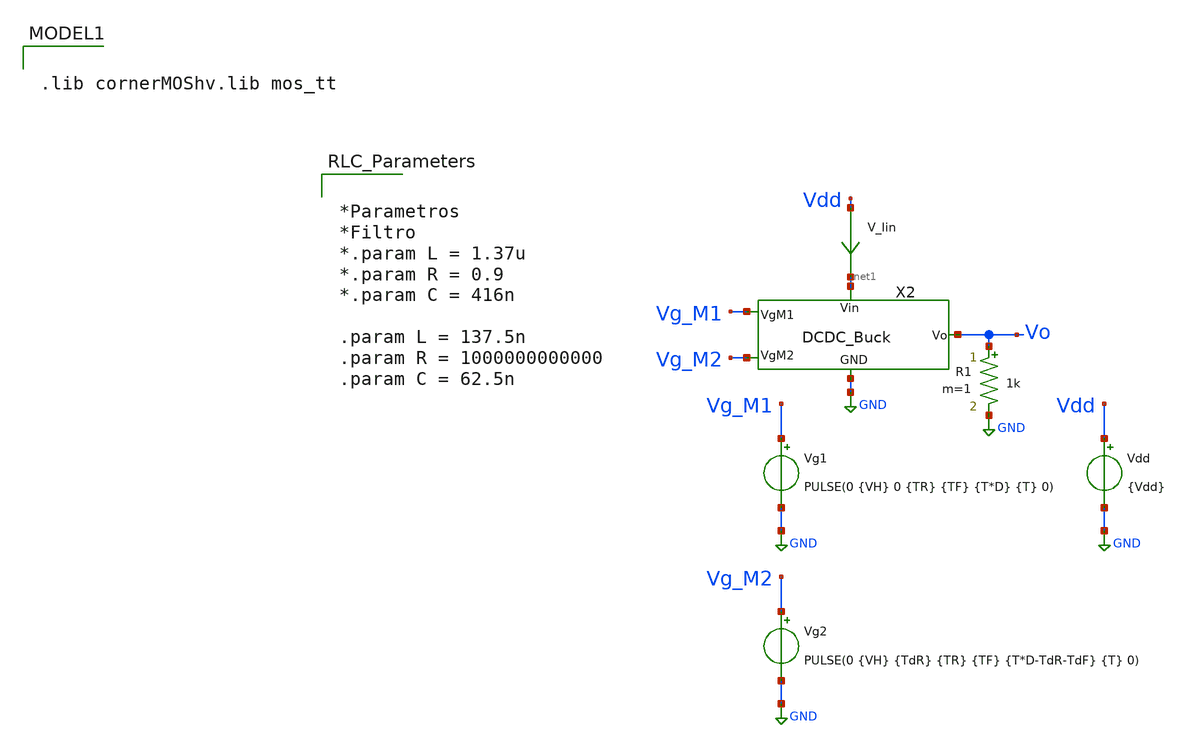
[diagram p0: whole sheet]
** sch_path: ChipUSM_AnalogTrack24/DCDCBuck/TB_DCDCBuck_SweepR.sch
**.subckt TB_DCDCBuck_SweepR
Vdd Vdd GND {Vdd}
Vg2 Vg_M2 GND PULSE(0 {VH} {TdR} {TR} {TF} {T*D-TdR-TdF} {T} 0)
Vg1 Vg_M1 GND PULSE(0 {VH} 0 {TR} {TF} {T*D} {T} 0)
V_Iin Vdd net1 0
.save i(v_iin)
R1 Vo GND 1k m=1
X2 Vg_M1 Vg_M2 net1 net2 Vo DCDC_Buck
**** begin user architecture code


.param temp=27
.param mult_M1 = 18000*2
.param w_M1 =10u
.param l_M1 = 0.4u
.param ng_M1 = 1

.param mult_M2 = 6000*2
.param w_M2 =10u
.param l_M2 =0.45u
.param ng_M2 =1







.param Vdd = 3.3
.param VH = 3.3
.param Del = 0

*.param D = 0.42
*.param T = 1u
*.param TR = 7n
*.param TF = 7n
*.param TdR = 0.1u
*.param TdF = 0.1u

*.param D = 0.6364
.param D = 0.55
.param T = 0.1u
.param TR = 10n
.param TF = 10n
.param TdR = 10n
.param TdF = 10n

.param temp = 27




.lib cornerMOShv.lib mos_tt



*Parametros
*Filtro
*.param L = 1.37u
*.param R = 0.9
*.param C = 416n

.param L = 137.5n
.param R = 1000000000000
.param C = 62.5n





.save all  @n.x1.xm1.nsg13_hv_pmos[ids]  @n.x1.xm2.nsg13_hv_nmos[ids]
.param SimTime = 5u
.param R = 0.6  ; Valor inicial de R

.control
reset
set color0 = white

* Barrido del parámetro R
foreach R_val 0.6 0.7 0.8 0.9 1.0 1.1 1.2
    print R_val
    alter R1 R_val  ; Cambiar el valor de R en cada iteración

    tran 1n 5u  ; Realizar la simulación transitoria

    let Io = i(v.x1.V_Io)
    let Id_M1 = @n.x1.xm1.nsg13_hv_pmos[ids]
    let Id_M2 = @n.x1.xm2.nsg13_hv_nmos[ids]
    let Po = Io*v(Vo)
    let I_in = i(V_Iin)
    let Pin = I_in*v(Vdd)
    let Vsd_M1 = v(Vdd) - v(x1.Vc)
    let Vds_M2 = v(x1.Vc)
    let P_M1 = Vsd_M1*Id_M1
    let P_M2 = -Vds_M2*Id_M2

    meas tran Vo_mean AVG v(Vo) from=4u to=5u
    meas tran Io_mean AVG Io from=4u to=5u
    meas tran Po_mean AVG Po from=4u to=5u
    meas tran Pin_mean AVG Pin from=4u to=5u
    meas tran P_M1_mean AVG P_M1 from=4u to=5u
    meas tran P_M2_mean AVG P_M2 from=4u to=5u

    let eff = 100*Po_mean/Pin_mean
    let loss_M1 = 100*P_M1_mean/Pin_mean
    let loss_M2 = 100*P_M2_mean/Pin_mean
    let sumaPot = eff + loss_M1 + loss_M2
    print eff loss_M1 loss_M2 sumaPot

    * Graficar los resultados por cada R_val
    plot Io i(v.x1.V_IL)
    *plot Id_M1 Id_M2
    *plot v(Vo)
    *plot Po Pin
    *plot v(x1.Vc)
    *plot v(Vg_M1) v(Vg_M2)

end  ; Fin del bucle foreach
.endc

.end





**** end user architecture code
**.ends

* expanding   symbol:
*+  /home/designer/shared/simulations/IHP-sg13g2/Simulaciones/Modulos/DCDC_Buck.sym # of pins=5
** sym_path: /home/designer/shared/simulations/IHP-sg13g2/Simulaciones/Modulos/DCDC_Buck.sym
** sch_path: /home/designer/shared/simulations/IHP-sg13g2/Simulaciones/Modulos/DCDC_Buck.sch
.subckt DCDC_Buck VgM1 VgM2 Vin GND Vo
*.iopin Vin
*.ipin VgM1
*.ipin VgM2
*.iopin Vo
*.iopin GND
XM2 GND VgM2 Vc GND sg13_hv_nmos w={w_M2} l={l_M2} ng={ng_M2} m={mult_M2} mm_ok=1
XM1 Vc VgM1 Vin Vin sg13_hv_pmos w={w_M1} l={l_M1} ng={ng_M1} m={mult_M1} mm_ok=1
L1 net2 net1 {L} m=1
C1 net1 GND {C} m=1
V_Io net1 Vo 0
.save i(v_io)
V_IL Vc net2 0
.save i(v_il)
R1 Vo GND {R} m=1
.ends

.GLOBAL GND
.end
